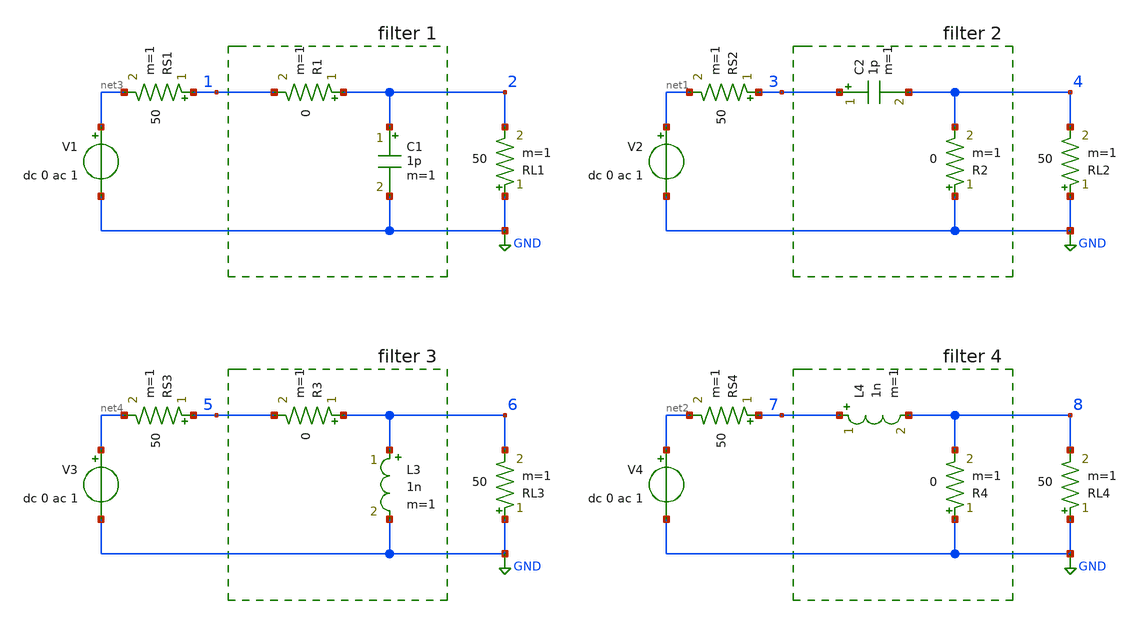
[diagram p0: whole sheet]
** sch_path: circuitos/exemplo03a.sch
**.subckt exemplo03a
V2 net1 GND dc 0 ac 1
RL2 GND 4 50 m=1
V3 net4 GND dc 0 ac 1
RL4 GND 8 50 m=1
RS2 3 net1 50 m=1
RS4 7 net2 50 m=1
C1 2 GND 1p m=1
V1 net3 GND dc 0 ac 1
RL1 GND 2 50 m=1
V4 net2 GND dc 0 ac 1
RL3 GND 6 50 m=1
L3 6 GND 1n m=1
RS1 1 net3 50 m=1
RS3 5 net4 50 m=1
R1 2 1 0 m=1
R3 6 5 0 m=1
L4 7 8 1n m=1
C2 3 4 1p m=1
R2 GND 4 0 m=1
R4 GND 8 0 m=1
**** begin user architecture code

.ac lin 1001 100 10G

**** end user architecture code
**.ends
.GLOBAL GND
.end
